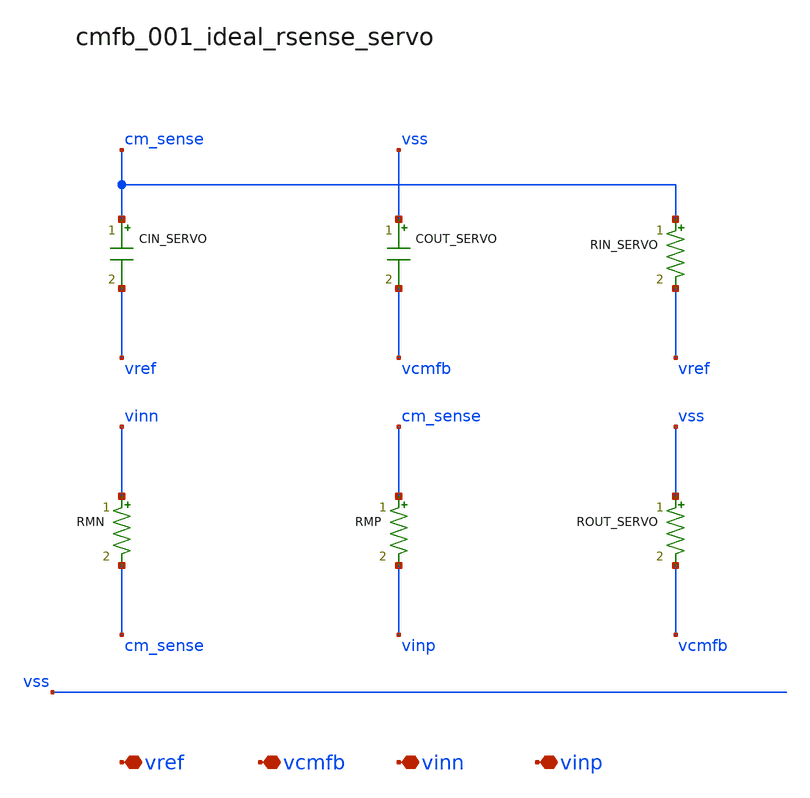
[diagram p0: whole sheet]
** sch_path: analog-db/raw/cmfb_001_ideal_rsense_servo/cmfb_001_ideal_rsense_servo_annotated.sch
**.subckt cmfb_001_ideal_rsense_servo_annotated vref vcmfb vinn vinp
*.iopin vref
*.iopin vcmfb
*.iopin vinn
*.iopin vinp
CIN_SERVO cm_sense vref 'cin_val' m=1
COUT_SERVO vss vcmfb 'cout_val' m=1
RIN_SERVO cm_sense vref 'rin_val' m=1
RMN vinn cm_sense 'x_dut_rmn_value' m=1
RMP cm_sense vinp 'x_dut_rmp_value' m=1
ROUT_SERVO vss vcmfb 'rout_val' m=1
**.ends
.end
